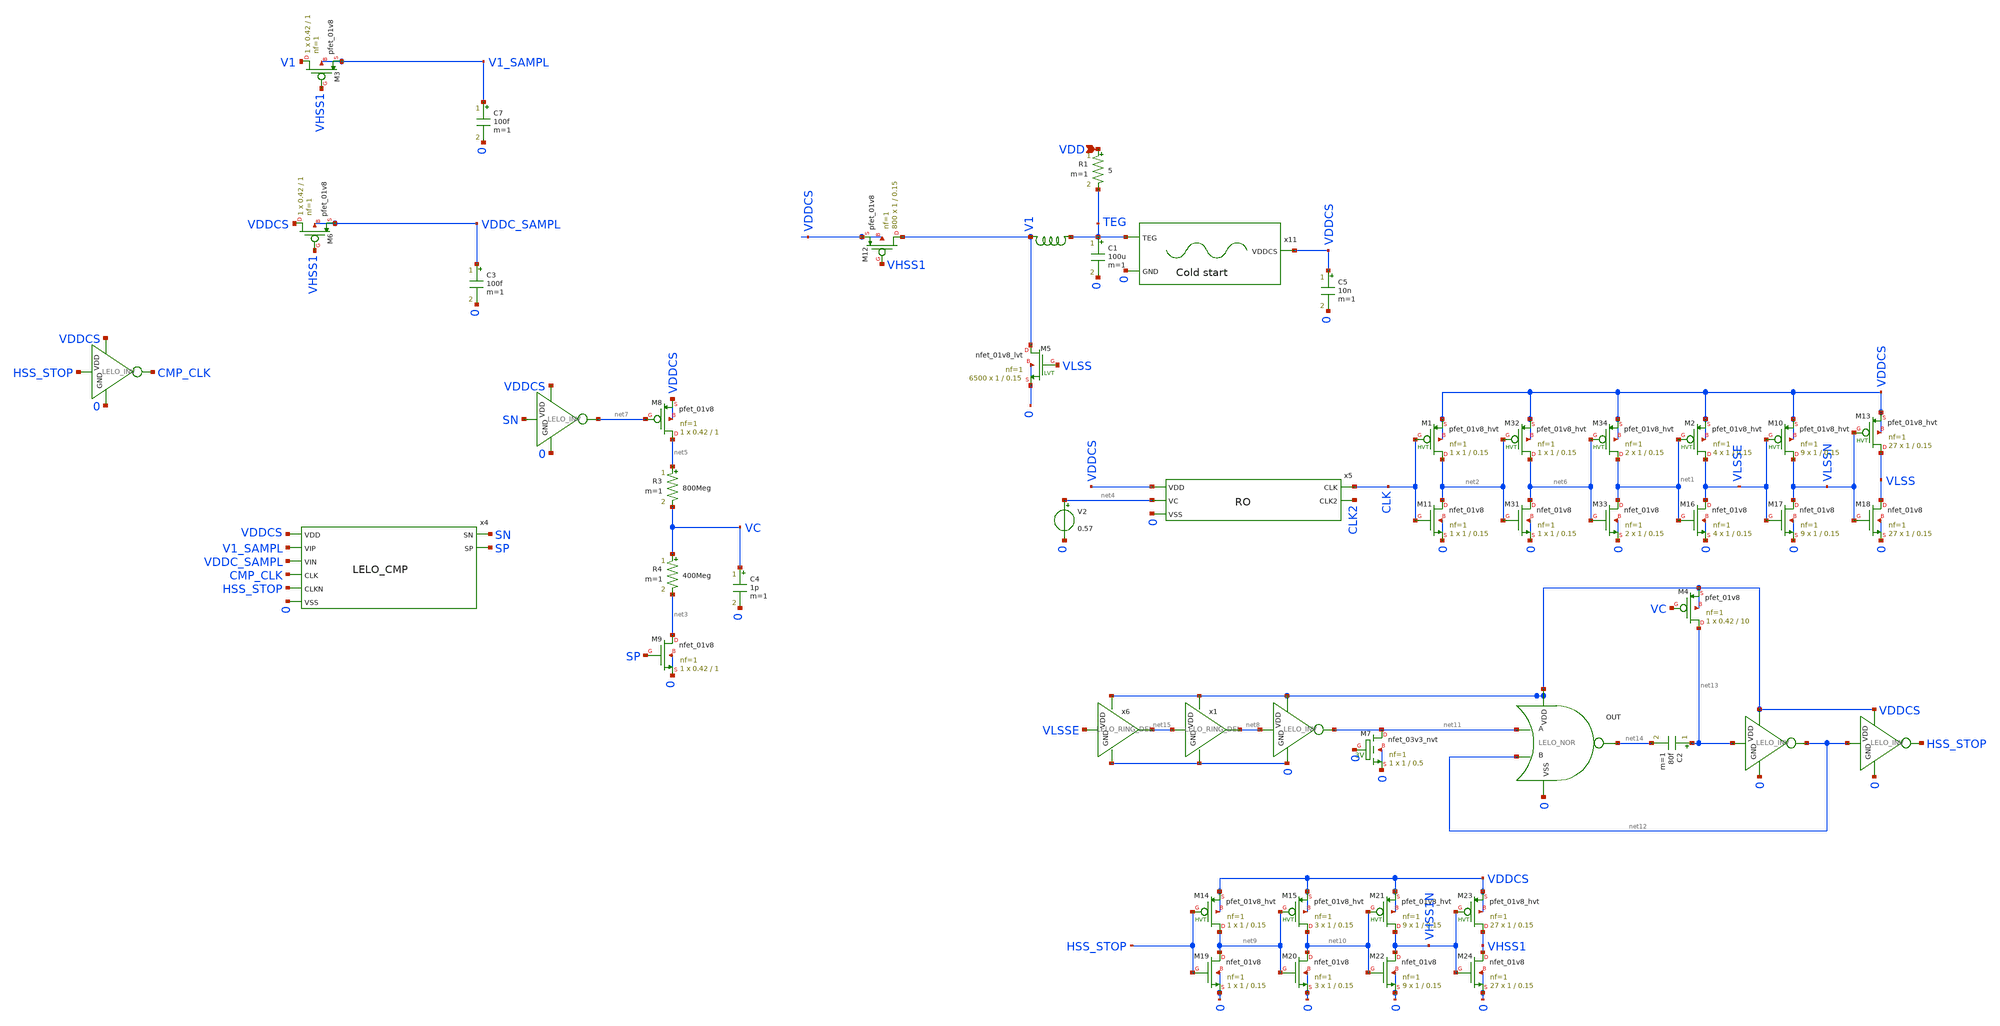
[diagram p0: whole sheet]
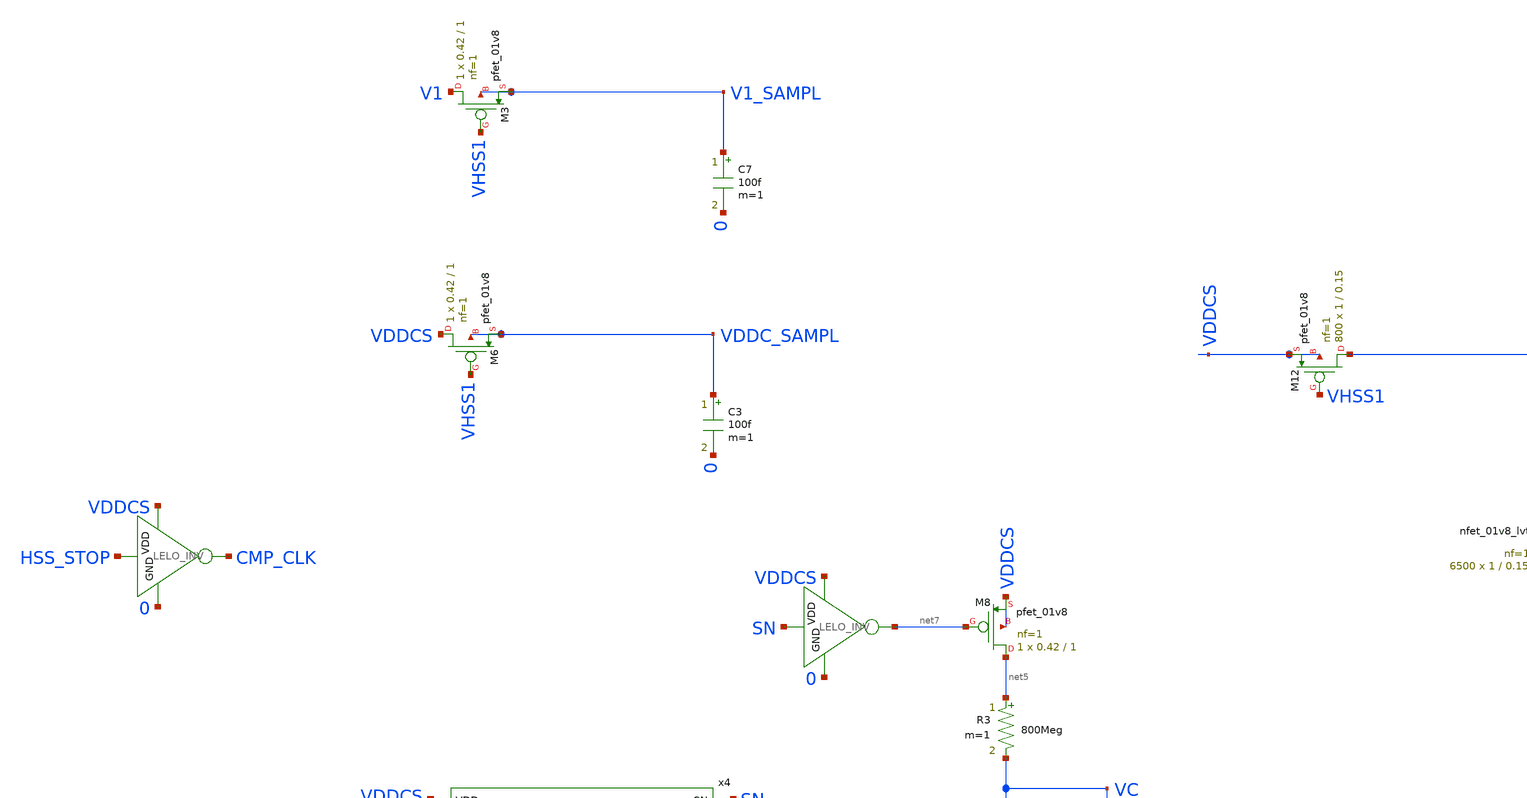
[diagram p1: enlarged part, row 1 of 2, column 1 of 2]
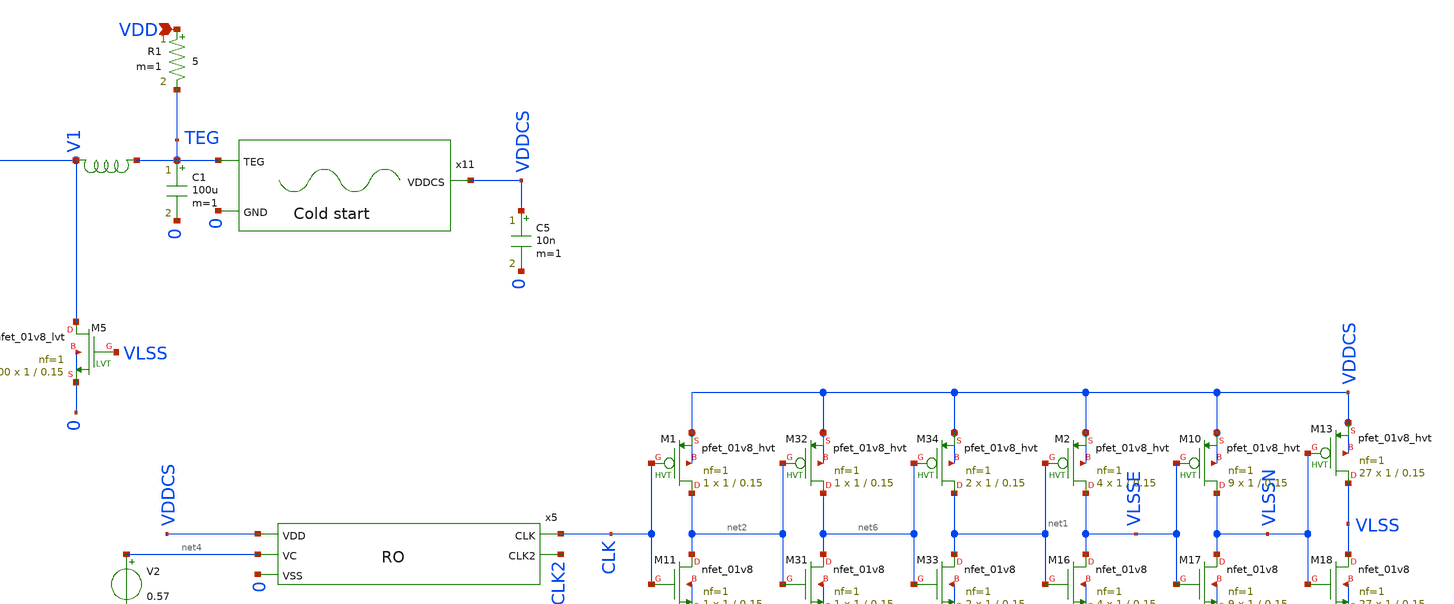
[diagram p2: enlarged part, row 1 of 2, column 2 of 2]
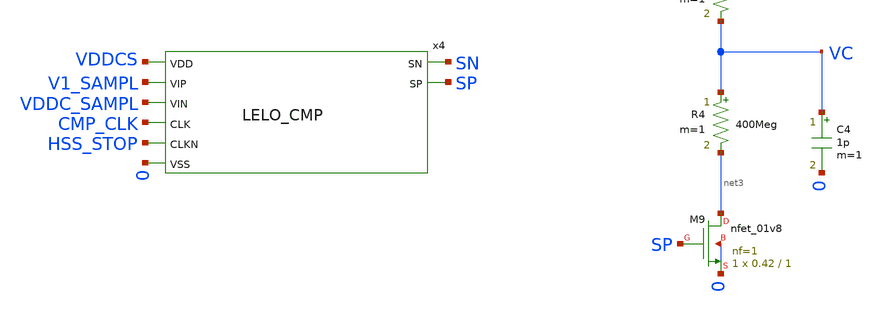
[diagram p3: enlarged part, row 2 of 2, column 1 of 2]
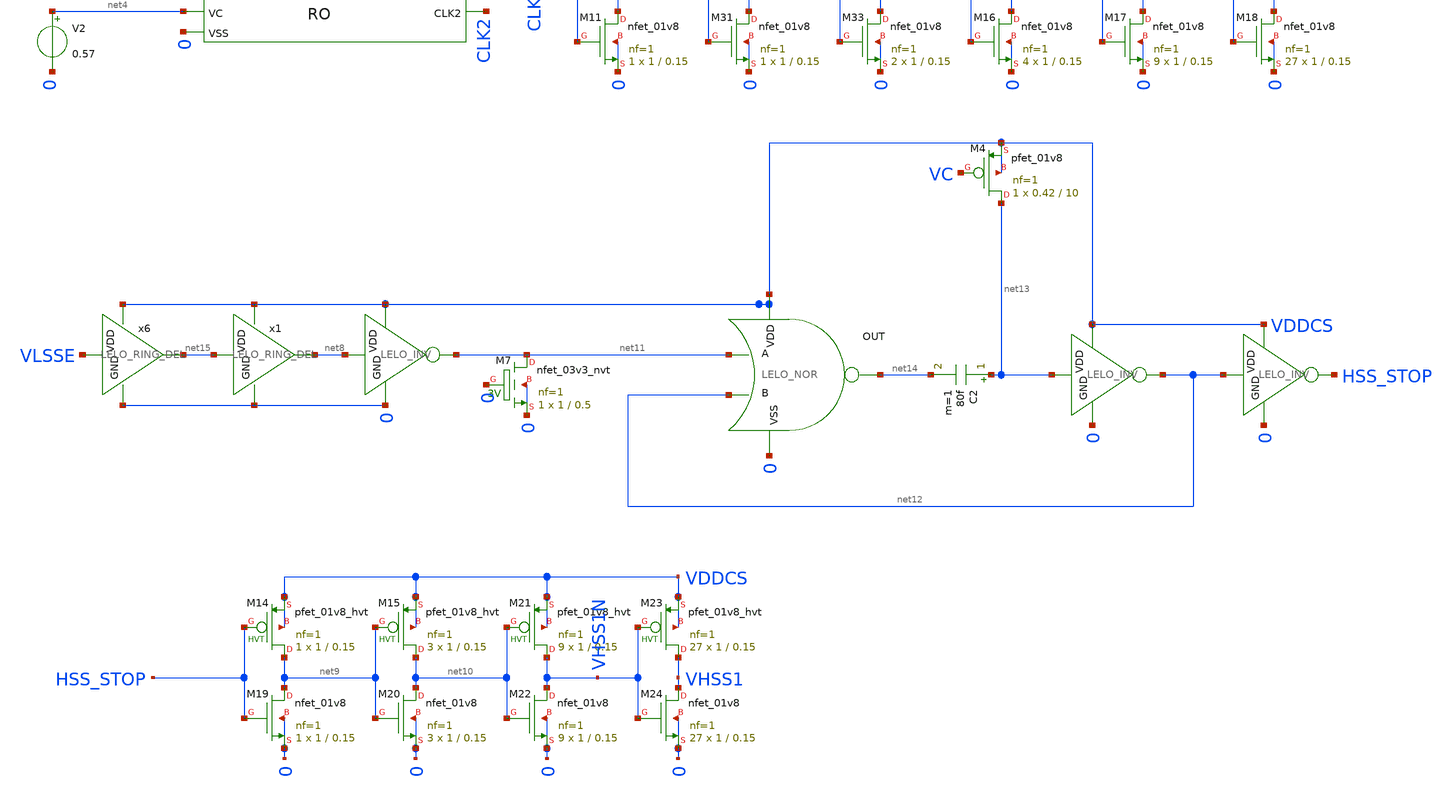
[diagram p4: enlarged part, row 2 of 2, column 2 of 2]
** sch_path: design/LELO_SVOD_SKY130A/LELO_EXSC.sch
**.subckt LELO_EXSC VDD
*.ipin VDD
R1 VDD TEG 5 m=1
C7 V1_SAMPL 0 100f m=1
x5 CLK CLK2 VDDCS net4 0 RO
XM12 V1 VHSS1 VDDCS VDDCS sky130_fd_pr__pfet_01v8 L=0.15 W=1 nf=1 ad='int((1 + 1)/2) * 1 / 1 * 0.29'
+ as='int((1 + 2)/2) * 1 / 1 * 0.29' pd='2*int((1 + 1)/2) * (1 / 1 + 0.29)' ps='2*int((1 + 2)/2) * (1 / 1 + 0.29)'
+ nrd='0.29 / 1 ' nrs='0.29 / 1 ' sa=0 sb=0 sd=0 mult=800 m=800
C1 TEG 0 100u m=1
XM5 V1 VLSS 0 0 sky130_fd_pr__nfet_01v8_lvt L=0.15 W=1 nf=1 ad='int((1 + 1)/2) * 1 / 1 * 0.29' as='int((1 + 2)/2) * 1 / 1 * 0.29'
+ pd='2*int((1 + 1)/2) * (1 / 1 + 0.29)' ps='2*int((1 + 2)/2) * (1 / 1 + 0.29)' nrd='0.29 / 1 ' nrs='0.29 / 1 '
+ sa=0 sb=0 sd=0 mult=6500 m=6500
x4 SN SP VDDCS V1_SAMPL VDDC_SAMPL CMP_CLK HSS_STOP 0 LELO_CMP
XM3 V1 VHSS1 V1_SAMPL V1_SAMPL sky130_fd_pr__pfet_01v8 L=1 W=0.42 nf=1 ad='int((1 + 1)/2) * 0.42 / 1 * 0.29'
+ as='int((1 + 2)/2) * 0.42 / 1 * 0.29' pd='2*int((1 + 1)/2) * (0.42 / 1 + 0.29)' ps='2*int((1 + 2)/2) * (0.42 / 1 + 0.29)'
+ nrd='0.29 / 0.42 ' nrs='0.29 / 0.42 ' sa=0 sb=0 sd=0 mult=1 m=1
C3 VDDC_SAMPL 0 100f m=1
XM6 VDDCS VHSS1 VDDC_SAMPL VDDC_SAMPL sky130_fd_pr__pfet_01v8 L=1 W=0.42 nf=1 ad='int((1 + 1)/2) * 0.42 / 1 * 0.29'
+ as='int((1 + 2)/2) * 0.42 / 1 * 0.29' pd='2*int((1 + 1)/2) * (0.42 / 1 + 0.29)' ps='2*int((1 + 2)/2) * (0.42 / 1 + 0.29)'
+ nrd='0.29 / 0.42 ' nrs='0.29 / 0.42 ' sa=0 sb=0 sd=0 mult=1 m=1
C4 VC 0 1p m=1
XM8 net5 net7 VDDCS VDDCS sky130_fd_pr__pfet_01v8 L=1 W=0.42 nf=1 ad='int((1 + 1)/2) * 0.42 / 1 * 0.29'
+ as='int((1 + 2)/2) * 0.42 / 1 * 0.29' pd='2*int((1 + 1)/2) * (0.42 / 1 + 0.29)' ps='2*int((1 + 2)/2) * (0.42 / 1 + 0.29)'
+ nrd='0.29 / 0.42 ' nrs='0.29 / 0.42 ' sa=0 sb=0 sd=0 mult=1 m=1
XM9 net3 SP 0 0 sky130_fd_pr__nfet_01v8 L=1 W=0.42 nf=1 ad='int((1 + 1)/2) * 0.42 / 1 * 0.29' as='int((1 + 2)/2) * 0.42 / 1 * 0.29'
+ pd='2*int((1 + 1)/2) * (0.42 / 1 + 0.29)' ps='2*int((1 + 2)/2) * (0.42 / 1 + 0.29)' nrd='0.29 / 0.42 '
+ nrs='0.29 / 0.42 ' sa=0 sb=0 sd=0 mult=1 m=1
V2 net4 0 0.57
x14 VDDCS HSS_STOP CMP_CLK 0 LELO_INV
R3 net5 VC 800Meg m=1
R4 VC net3 400Meg m=1
XM11 net2 CLK 0 0 sky130_fd_pr__nfet_01v8 L=0.15 W=1 nf=1 ad='int((1 + 1)/2) * 1 / 1 * 0.29' as='int((1 + 2)/2) * 1 / 1 * 0.29'
+ pd='2*int((1 + 1)/2) * (1 / 1 + 0.29)' ps='2*int((1 + 2)/2) * (1 / 1 + 0.29)' nrd='0.29 / 1 ' nrs='0.29 / 1 '
+ sa=0 sb=0 sd=0 mult=1 m=1
XM16 VLSSE net1 0 0 sky130_fd_pr__nfet_01v8 L=0.15 W=1 nf=1 ad='int((1 + 1)/2) * 1 / 1 * 0.29' as='int((1 + 2)/2) * 1 / 1 * 0.29'
+ pd='2*int((1 + 1)/2) * (1 / 1 + 0.29)' ps='2*int((1 + 2)/2) * (1 / 1 + 0.29)' nrd='0.29 / 1 ' nrs='0.29 / 1 '
+ sa=0 sb=0 sd=0 mult=4 m=4
XM17 VLSSN VLSSE 0 0 sky130_fd_pr__nfet_01v8 L=0.15 W=1 nf=1 ad='int((1 + 1)/2) * 1 / 1 * 0.29' as='int((1 + 2)/2) * 1 / 1 * 0.29'
+ pd='2*int((1 + 1)/2) * (1 / 1 + 0.29)' ps='2*int((1 + 2)/2) * (1 / 1 + 0.29)' nrd='0.29 / 1 ' nrs='0.29 / 1 '
+ sa=0 sb=0 sd=0 mult=9 m=9
XM18 VLSS VLSSN 0 0 sky130_fd_pr__nfet_01v8 L=0.15 W=1 nf=1 ad='int((1 + 1)/2) * 1 / 1 * 0.29' as='int((1 + 2)/2) * 1 / 1 * 0.29'
+ pd='2*int((1 + 1)/2) * (1 / 1 + 0.29)' ps='2*int((1 + 2)/2) * (1 / 1 + 0.29)' nrd='0.29 / 1 ' nrs='0.29 / 1 '
+ sa=0 sb=0 sd=0 mult=27 m=27
XM1 net2 CLK VDDCS VDDCS sky130_fd_pr__pfet_01v8_hvt L=0.15 W=1 nf=1 ad='int((1 + 1)/2) * 1 / 1 * 0.29'
+ as='int((1 + 2)/2) * 1 / 1 * 0.29' pd='2*int((1 + 1)/2) * (1 / 1 + 0.29)' ps='2*int((1 + 2)/2) * (1 / 1 + 0.29)'
+ nrd='0.29 / 1 ' nrs='0.29 / 1 ' sa=0 sb=0 sd=0 mult=1 m=1
XM2 VLSSE net1 VDDCS VDDCS sky130_fd_pr__pfet_01v8_hvt L=0.15 W=1 nf=1 ad='int((1 + 1)/2) * 1 / 1 * 0.29'
+ as='int((1 + 2)/2) * 1 / 1 * 0.29' pd='2*int((1 + 1)/2) * (1 / 1 + 0.29)' ps='2*int((1 + 2)/2) * (1 / 1 + 0.29)'
+ nrd='0.29 / 1 ' nrs='0.29 / 1 ' sa=0 sb=0 sd=0 mult=4 m=4
XM10 VLSSN VLSSE VDDCS VDDCS sky130_fd_pr__pfet_01v8_hvt L=0.15 W=1 nf=1 ad='int((1 + 1)/2) * 1 / 1 * 0.29'
+ as='int((1 + 2)/2) * 1 / 1 * 0.29' pd='2*int((1 + 1)/2) * (1 / 1 + 0.29)' ps='2*int((1 + 2)/2) * (1 / 1 + 0.29)'
+ nrd='0.29 / 1 ' nrs='0.29 / 1 ' sa=0 sb=0 sd=0 mult=9 m=9
XM13 VLSS VLSSN VDDCS VDDCS sky130_fd_pr__pfet_01v8_hvt L=0.15 W=1 nf=1 ad='int((1 + 1)/2) * 1 / 1 * 0.29'
+ as='int((1 + 2)/2) * 1 / 1 * 0.29' pd='2*int((1 + 1)/2) * (1 / 1 + 0.29)' ps='2*int((1 + 2)/2) * (1 / 1 + 0.29)'
+ nrd='0.29 / 1 ' nrs='0.29 / 1 ' sa=0 sb=0 sd=0 mult=27 m=27
XM31 net6 net2 0 0 sky130_fd_pr__nfet_01v8 L=0.15 W=1 nf=1 ad='int((1 + 1)/2) * 1 / 1 * 0.29' as='int((1 + 2)/2) * 1 / 1 * 0.29'
+ pd='2*int((1 + 1)/2) * (1 / 1 + 0.29)' ps='2*int((1 + 2)/2) * (1 / 1 + 0.29)' nrd='0.29 / 1 ' nrs='0.29 / 1 '
+ sa=0 sb=0 sd=0 mult=1 m=1
XM32 net6 net2 VDDCS VDDCS sky130_fd_pr__pfet_01v8_hvt L=0.15 W=1 nf=1 ad='int((1 + 1)/2) * 1 / 1 * 0.29'
+ as='int((1 + 2)/2) * 1 / 1 * 0.29' pd='2*int((1 + 1)/2) * (1 / 1 + 0.29)' ps='2*int((1 + 2)/2) * (1 / 1 + 0.29)'
+ nrd='0.29 / 1 ' nrs='0.29 / 1 ' sa=0 sb=0 sd=0 mult=1 m=1
XM33 net1 net6 0 0 sky130_fd_pr__nfet_01v8 L=0.15 W=1 nf=1 ad='int((1 + 1)/2) * 1 / 1 * 0.29' as='int((1 + 2)/2) * 1 / 1 * 0.29'
+ pd='2*int((1 + 1)/2) * (1 / 1 + 0.29)' ps='2*int((1 + 2)/2) * (1 / 1 + 0.29)' nrd='0.29 / 1 ' nrs='0.29 / 1 '
+ sa=0 sb=0 sd=0 mult=2 m=2
XM34 net1 net6 VDDCS VDDCS sky130_fd_pr__pfet_01v8_hvt L=0.15 W=1 nf=1 ad='int((1 + 1)/2) * 1 / 1 * 0.29'
+ as='int((1 + 2)/2) * 1 / 1 * 0.29' pd='2*int((1 + 1)/2) * (1 / 1 + 0.29)' ps='2*int((1 + 2)/2) * (1 / 1 + 0.29)'
+ nrd='0.29 / 1 ' nrs='0.29 / 1 ' sa=0 sb=0 sd=0 mult=2 m=2
x7 TEG V1 XGL6030-822_sat
x10 VDDCS SN net7 0 LELO_INV
C5 VDDCS 0 10n m=1
x11 TEG VDDCS 0 LELO_COLD_START
x16 VDDCS net12 HSS_STOP 0 LELO_INV
x9 VDDCS net8 net11 0 LELO_INV
XM19 net9 HSS_STOP 0 0 sky130_fd_pr__nfet_01v8 L=0.15 W=1 nf=1 ad='int((1 + 1)/2) * 1 / 1 * 0.29' as='int((1 + 2)/2) * 1 / 1 * 0.29'
+ pd='2*int((1 + 1)/2) * (1 / 1 + 0.29)' ps='2*int((1 + 2)/2) * (1 / 1 + 0.29)' nrd='0.29 / 1 ' nrs='0.29 / 1 '
+ sa=0 sb=0 sd=0 mult=1 m=1
XM20 net10 net9 0 0 sky130_fd_pr__nfet_01v8 L=0.15 W=1 nf=1 ad='int((1 + 1)/2) * 1 / 1 * 0.29' as='int((1 + 2)/2) * 1 / 1 * 0.29'
+ pd='2*int((1 + 1)/2) * (1 / 1 + 0.29)' ps='2*int((1 + 2)/2) * (1 / 1 + 0.29)' nrd='0.29 / 1 ' nrs='0.29 / 1 '
+ sa=0 sb=0 sd=0 mult=3 m=3
XM22 VHSS1N net10 0 0 sky130_fd_pr__nfet_01v8 L=0.15 W=1 nf=1 ad='int((1 + 1)/2) * 1 / 1 * 0.29' as='int((1 + 2)/2) * 1 / 1 * 0.29'
+ pd='2*int((1 + 1)/2) * (1 / 1 + 0.29)' ps='2*int((1 + 2)/2) * (1 / 1 + 0.29)' nrd='0.29 / 1 ' nrs='0.29 / 1 '
+ sa=0 sb=0 sd=0 mult=9 m=9
XM24 VHSS1 VHSS1N 0 0 sky130_fd_pr__nfet_01v8 L=0.15 W=1 nf=1 ad='int((1 + 1)/2) * 1 / 1 * 0.29' as='int((1 + 2)/2) * 1 / 1 * 0.29'
+ pd='2*int((1 + 1)/2) * (1 / 1 + 0.29)' ps='2*int((1 + 2)/2) * (1 / 1 + 0.29)' nrd='0.29 / 1 ' nrs='0.29 / 1 '
+ sa=0 sb=0 sd=0 mult=27 m=27
XM14 net9 HSS_STOP VDDCS VDDCS sky130_fd_pr__pfet_01v8_hvt L=0.15 W=1 nf=1 ad='int((1 + 1)/2) * 1 / 1 * 0.29'
+ as='int((1 + 2)/2) * 1 / 1 * 0.29' pd='2*int((1 + 1)/2) * (1 / 1 + 0.29)' ps='2*int((1 + 2)/2) * (1 / 1 + 0.29)'
+ nrd='0.29 / 1 ' nrs='0.29 / 1 ' sa=0 sb=0 sd=0 mult=1 m=1
XM15 net10 net9 VDDCS VDDCS sky130_fd_pr__pfet_01v8_hvt L=0.15 W=1 nf=1 ad='int((1 + 1)/2) * 1 / 1 * 0.29'
+ as='int((1 + 2)/2) * 1 / 1 * 0.29' pd='2*int((1 + 1)/2) * (1 / 1 + 0.29)' ps='2*int((1 + 2)/2) * (1 / 1 + 0.29)'
+ nrd='0.29 / 1 ' nrs='0.29 / 1 ' sa=0 sb=0 sd=0 mult=3 m=3
XM21 VHSS1N net10 VDDCS VDDCS sky130_fd_pr__pfet_01v8_hvt L=0.15 W=1 nf=1 ad='int((1 + 1)/2) * 1 / 1 * 0.29'
+ as='int((1 + 2)/2) * 1 / 1 * 0.29' pd='2*int((1 + 1)/2) * (1 / 1 + 0.29)' ps='2*int((1 + 2)/2) * (1 / 1 + 0.29)'
+ nrd='0.29 / 1 ' nrs='0.29 / 1 ' sa=0 sb=0 sd=0 mult=9 m=9
XM23 VHSS1 VHSS1N VDDCS VDDCS sky130_fd_pr__pfet_01v8_hvt L=0.15 W=1 nf=1 ad='int((1 + 1)/2) * 1 / 1 * 0.29'
+ as='int((1 + 2)/2) * 1 / 1 * 0.29' pd='2*int((1 + 1)/2) * (1 / 1 + 0.29)' ps='2*int((1 + 2)/2) * (1 / 1 + 0.29)'
+ nrd='0.29 / 1 ' nrs='0.29 / 1 ' sa=0 sb=0 sd=0 mult=27 m=27
x2 VDDCS net14 net11 net12 0 LELO_NOR
C2 net13 net14 80f m=1
x3 VDDCS net13 net12 0 LELO_INV
XM4 net13 VC VDDCS VDDCS sky130_fd_pr__pfet_01v8 L=10 W=0.42 nf=1 ad='int((1 + 1)/2) * 0.42 / 1 * 0.29'
+ as='int((1 + 2)/2) * 0.42 / 1 * 0.29' pd='2*int((1 + 1)/2) * (0.42 / 1 + 0.29)' ps='2*int((1 + 2)/2) * (0.42 / 1 + 0.29)'
+ nrd='0.29 / 0.42 ' nrs='0.29 / 0.42 ' sa=0 sb=0 sd=0 mult=1 m=1
x1 VDDCS net15 net8 0 LELO_RING_DEL
x6 VDDCS VLSSE net15 0 LELO_RING_DEL
XM7 net11 0 0 0 sky130_fd_pr__nfet_03v3_nvt L=0.5 W=1 nf=1 ad='int((1 + 1)/2) * 1 / 1 * 0.29' as='int((1 + 2)/2) * 1 / 1 * 0.29'
+ pd='2*int((1 + 1)/2) * (1 / 1 + 0.29)' ps='2*int((1 + 2)/2) * (1 / 1 + 0.29)' nrd='0.29 / 1 ' nrs='0.29 / 1 '
+ sa=0 sb=0 sd=0 mult=1 m=1
**.ends

* expanding   symbol:  LELO_SVOD_SKY130A/RO.sym # of pins=5
** sym_path: design/LELO_SVOD_SKY130A/RO.sym
** sch_path: design/LELO_SVOD_SKY130A/RO.sch
.subckt RO CLK CLK2 VDD VC VSS
*.opin CLK
*.ipin VSS
*.opin CLK2
*.ipin VDD
*.ipin VC
x1 VDD VC2 CLK net1 VC VSS LELO_RING_DEL_VC
x2 VDD VC2 net1 net2 VC VSS LELO_RING_DEL_VC
x3 VDD VC2 net2 net3 VC VSS LELO_RING_DEL_VC
x4 VDD VC2 net3 CLK2 VC VSS LELO_RING_DEL_VC
x5 VDD VC2 CLK2 net4 VC VSS LELO_RING_DEL_VC
x6 VDD VC2 net4 net5 VC VSS LELO_RING_DEL_VC
x7 VDD VC2 net5 CLK VC VSS LELO_RING_DEL_VC
XM1 VC2 VC VSS VSS sky130_fd_pr__nfet_01v8 L=5 W=0.42 nf=1 ad='int((1 + 1)/2) * 0.42 / 1 * 0.29' as='int((1 + 2)/2) * 0.42 / 1 * 0.29'
+ pd='2*int((1 + 1)/2) * (0.42 / 1 + 0.29)' ps='2*int((1 + 2)/2) * (0.42 / 1 + 0.29)' nrd='0.29 / 0.42 '
+ nrs='0.29 / 0.42 ' sa=0 sb=0 sd=0 mult=1 m=1
XM2 VC2 VC2 VDD VDD sky130_fd_pr__pfet_01v8 L=5 W=0.42 nf=1 ad='int((1 + 1)/2) * 0.42 / 1 * 0.29' as='int((1 + 2)/2) * 0.42 / 1 * 0.29'
+ pd='2*int((1 + 1)/2) * (0.42 / 1 + 0.29)' ps='2*int((1 + 2)/2) * (0.42 / 1 + 0.29)' nrd='0.29 / 0.42 '
+ nrs='0.29 / 0.42 ' sa=0 sb=0 sd=0 mult=1 m=1
.ends


* expanding   symbol:  LELO_SVOD_SKY130A/LELO_CMP.sym # of pins=8
** sym_path: design/LELO_SVOD_SKY130A/LELO_CMP.sym
** sch_path: design/LELO_SVOD_SKY130A/LELO_CMP.sch
.subckt LELO_CMP SN SP VDD VIP VIN CLK CLKN VSS
*.ipin VIP
*.ipin VIN
*.ipin CLK
*.ipin CLKN
*.ipin VDD
*.ipin VSS
*.opin SN
*.opin SP
XM2 SN net3 net5 VDD sky130_fd_pr__pfet_01v8_lvt L=0.44 W=1.92 nf=2 ad='int((2 + 1)/2) * 1.92 / 2 * 0.29'
+ as='int((2 + 2)/2) * 1.92 / 2 * 0.29' pd='2*int((2 + 1)/2) * (1.92 / 2 + 0.29)' ps='2*int((2 + 2)/2) * (1.92 / 2 + 0.29)'
+ nrd='0.29 / 1.92 ' nrs='0.29 / 1.92 ' sa=0 sb=0 sd=0 mult=3 m=3
XM1 SP net2 net6 VDD sky130_fd_pr__pfet_01v8_lvt L=0.44 W=1.92 nf=2 ad='int((2 + 1)/2) * 1.92 / 2 * 0.29'
+ as='int((2 + 2)/2) * 1.92 / 2 * 0.29' pd='2*int((2 + 1)/2) * (1.92 / 2 + 0.29)' ps='2*int((2 + 2)/2) * (1.92 / 2 + 0.29)'
+ nrd='0.29 / 1.92 ' nrs='0.29 / 1.92 ' sa=0 sb=0 sd=0 mult=3 m=3
XM3 net2 VIP net1 VSS sky130_fd_pr__nfet_01v8_lvt L=0.44 W=6.4 nf=1 ad='int((1 + 1)/2) * 6.4 / 1 * 0.29'
+ as='int((1 + 2)/2) * 6.4 / 1 * 0.29' pd='2*int((1 + 1)/2) * (6.4 / 1 + 0.29)' ps='2*int((1 + 2)/2) * (6.4 / 1 + 0.29)'
+ nrd='0.29 / 6.4 ' nrs='0.29 / 6.4 ' sa=0 sb=0 sd=0 mult=1 m=1
XM4 net3 VIN net1 VSS sky130_fd_pr__nfet_01v8_lvt L=0.44 W=6.4 nf=1 ad='int((1 + 1)/2) * 6.4 / 1 * 0.29'
+ as='int((1 + 2)/2) * 6.4 / 1 * 0.29' pd='2*int((1 + 1)/2) * (6.4 / 1 + 0.29)' ps='2*int((1 + 2)/2) * (6.4 / 1 + 0.29)'
+ nrd='0.29 / 6.4 ' nrs='0.29 / 6.4 ' sa=0 sb=0 sd=0 mult=1 m=1
XM5 net3 CLK VDD VDD sky130_fd_pr__pfet_01v8_lvt L=0.94 W=1.92 nf=2 ad='int((2 + 1)/2) * 1.92 / 2 * 0.29'
+ as='int((2 + 2)/2) * 1.92 / 2 * 0.29' pd='2*int((2 + 1)/2) * (1.92 / 2 + 0.29)' ps='2*int((2 + 2)/2) * (1.92 / 2 + 0.29)'
+ nrd='0.29 / 1.92 ' nrs='0.29 / 1.92 ' sa=0 sb=0 sd=0 mult=1 m=1
XM6 net6 SN VDD VDD sky130_fd_pr__pfet_01v8_lvt L=0.94 W=1.92 nf=2 ad='int((2 + 1)/2) * 1.92 / 2 * 0.29'
+ as='int((2 + 2)/2) * 1.92 / 2 * 0.29' pd='2*int((2 + 1)/2) * (1.92 / 2 + 0.29)' ps='2*int((2 + 2)/2) * (1.92 / 2 + 0.29)'
+ nrd='0.29 / 1.92 ' nrs='0.29 / 1.92 ' sa=0 sb=0 sd=0 mult=1 m=1
XM7 net5 SP VDD VDD sky130_fd_pr__pfet_01v8_lvt L=0.94 W=1.92 nf=2 ad='int((2 + 1)/2) * 1.92 / 2 * 0.29'
+ as='int((2 + 2)/2) * 1.92 / 2 * 0.29' pd='2*int((2 + 1)/2) * (1.92 / 2 + 0.29)' ps='2*int((2 + 2)/2) * (1.92 / 2 + 0.29)'
+ nrd='0.29 / 1.92 ' nrs='0.29 / 1.92 ' sa=0 sb=0 sd=0 mult=1 m=1
XM8 net2 CLK VDD VDD sky130_fd_pr__pfet_01v8_lvt L=0.94 W=1.92 nf=2 ad='int((2 + 1)/2) * 1.92 / 2 * 0.29'
+ as='int((2 + 2)/2) * 1.92 / 2 * 0.29' pd='2*int((2 + 1)/2) * (1.92 / 2 + 0.29)' ps='2*int((2 + 2)/2) * (1.92 / 2 + 0.29)'
+ nrd='0.29 / 1.92 ' nrs='0.29 / 1.92 ' sa=0 sb=0 sd=0 mult=1 m=1
XM9 net1 CLK net4 VSS sky130_fd_pr__nfet_01v8 L=0.94 W=1.92 nf=2 ad='int((2 + 1)/2) * 1.92 / 2 * 0.29'
+ as='int((2 + 2)/2) * 1.92 / 2 * 0.29' pd='2*int((2 + 1)/2) * (1.92 / 2 + 0.29)' ps='2*int((2 + 2)/2) * (1.92 / 2 + 0.29)'
+ nrd='0.29 / 1.92 ' nrs='0.29 / 1.92 ' sa=0 sb=0 sd=0 mult=1 m=1
XM10 net4 CLK VSS VSS sky130_fd_pr__nfet_01v8 L=0.94 W=1.92 nf=2 ad='int((2 + 1)/2) * 1.92 / 2 * 0.29'
+ as='int((2 + 2)/2) * 1.92 / 2 * 0.29' pd='2*int((2 + 1)/2) * (1.92 / 2 + 0.29)' ps='2*int((2 + 2)/2) * (1.92 / 2 + 0.29)'
+ nrd='0.29 / 1.92 ' nrs='0.29 / 1.92 ' sa=0 sb=0 sd=0 mult=1 m=1
XM11 SN CLKN VSS VSS sky130_fd_pr__nfet_01v8 L=0.94 W=1.92 nf=2 ad='int((2 + 1)/2) * 1.92 / 2 * 0.29'
+ as='int((2 + 2)/2) * 1.92 / 2 * 0.29' pd='2*int((2 + 1)/2) * (1.92 / 2 + 0.29)' ps='2*int((2 + 2)/2) * (1.92 / 2 + 0.29)'
+ nrd='0.29 / 1.92 ' nrs='0.29 / 1.92 ' sa=0 sb=0 sd=0 mult=1 m=1
XM12 SP SN VSS VSS sky130_fd_pr__nfet_01v8 L=0.94 W=1.92 nf=2 ad='int((2 + 1)/2) * 1.92 / 2 * 0.29' as='int((2 + 2)/2) * 1.92 / 2 * 0.29'
+ pd='2*int((2 + 1)/2) * (1.92 / 2 + 0.29)' ps='2*int((2 + 2)/2) * (1.92 / 2 + 0.29)' nrd='0.29 / 1.92 '
+ nrs='0.29 / 1.92 ' sa=0 sb=0 sd=0 mult=1 m=1
XM13 SN SP VSS VSS sky130_fd_pr__nfet_01v8 L=0.94 W=1.92 nf=2 ad='int((2 + 1)/2) * 1.92 / 2 * 0.29' as='int((2 + 2)/2) * 1.92 / 2 * 0.29'
+ pd='2*int((2 + 1)/2) * (1.92 / 2 + 0.29)' ps='2*int((2 + 2)/2) * (1.92 / 2 + 0.29)' nrd='0.29 / 1.92 '
+ nrs='0.29 / 1.92 ' sa=0 sb=0 sd=0 mult=1 m=1
XM14 SP CLKN VSS VSS sky130_fd_pr__nfet_01v8 L=0.94 W=1.92 nf=2 ad='int((2 + 1)/2) * 1.92 / 2 * 0.29'
+ as='int((2 + 2)/2) * 1.92 / 2 * 0.29' pd='2*int((2 + 1)/2) * (1.92 / 2 + 0.29)' ps='2*int((2 + 2)/2) * (1.92 / 2 + 0.29)'
+ nrd='0.29 / 1.92 ' nrs='0.29 / 1.92 ' sa=0 sb=0 sd=0 mult=1 m=1
.ends


* expanding   symbol:  LELO_SVOD_SKY130A/LELO_INV.sym # of pins=4
** sym_path: design/LELO_SVOD_SKY130A/LELO_INV.sym
** sch_path: design/LELO_SVOD_SKY130A/LELO_INV.sch
.subckt LELO_INV VDD VIN VOUT GND
*.ipin VIN
*.ipin VDD
*.ipin GND
*.opin VOUT
XM1 VOUT VIN GND GND sky130_fd_pr__nfet_01v8_lvt L=0.15 W=1 nf=1 ad='int((1 + 1)/2) * 1 / 1 * 0.29' as='int((1 + 2)/2) * 1 / 1 * 0.29'
+ pd='2*int((1 + 1)/2) * (1 / 1 + 0.29)' ps='2*int((1 + 2)/2) * (1 / 1 + 0.29)' nrd='0.29 / 1 ' nrs='0.29 / 1 '
+ sa=0 sb=0 sd=0 mult=1 m=1
XM2 VOUT VIN VDD VDD sky130_fd_pr__pfet_01v8_lvt L=0.35 W=1 nf=1 ad='int((1 + 1)/2) * 1 / 1 * 0.29' as='int((1 + 2)/2) * 1 / 1 * 0.29'
+ pd='2*int((1 + 1)/2) * (1 / 1 + 0.29)' ps='2*int((1 + 2)/2) * (1 / 1 + 0.29)' nrd='0.29 / 1 ' nrs='0.29 / 1 '
+ sa=0 sb=0 sd=0 mult=2 m=2
.ends


* expanding   symbol:  LELO_SVOD_SKY130A/XGL6030-822_sat.sym # of pins=2
** sym_path: design/LELO_SVOD_SKY130A/XGL6030-822_sat.sym

.subckt XGL6030-822_sat port1 port2
X1 port1 port2 Model1C R1=5 R2=0.04 C= 15.2p K1=0.000001 K2=2 K3= 8.2u K4=0.000001 K5=0.000001
+ L=8.1093E-06 Is=13.9236 a=0.7109 L_Z0=0 L_EL=0 L_F0=0E6 PkZ=7057.14402
.ends XGL6030-822_sat


* expanding   symbol:  LELO_SVOD_SKY130A/LELO_COLD_START.sym # of pins=3
** sym_path: design/LELO_SVOD_SKY130A/LELO_COLD_START.sym
** sch_path: design/LELO_SVOD_SKY130A/LELO_COLD_START.sch
.subckt LELO_COLD_START TEG VDDCS GND
*.ipin GND
*.ipin TEG
*.opin VDDCS
C2 net4 VG1 110p m=1
x1 VG2 net2 1812PS-564_imp
x2 net1 VG1 1812PS-564_imp
C4 net3 VG2 110p m=1
XM1 net1 VG2 GND GND sky130_fd_pr__nfet_20v0_zvt W=60 L=0.5 m=100
XM2 net2 VG1 GND GND sky130_fd_pr__nfet_20v0_zvt W=60 L=0.5 m=100
XM3 TEG TEG net4 TEG sky130_fd_pr__nfet_01v8_lvt L=0.15 W=10 nf=1 ad='int((1 + 1)/2) * 10 / 1 * 0.29'
+ as='int((1 + 2)/2) * 10 / 1 * 0.29' pd='2*int((1 + 1)/2) * (10 / 1 + 0.29)' ps='2*int((1 + 2)/2) * (10 / 1 + 0.29)'
+ nrd='0.29 / 10 ' nrs='0.29 / 10 ' sa=0 sb=0 sd=0 mult=1 m=1
XM7 net4 net4 net3 net4 sky130_fd_pr__nfet_01v8_lvt L=0.15 W=10 nf=1 ad='int((1 + 1)/2) * 10 / 1 * 0.29'
+ as='int((1 + 2)/2) * 10 / 1 * 0.29' pd='2*int((1 + 1)/2) * (10 / 1 + 0.29)' ps='2*int((1 + 2)/2) * (10 / 1 + 0.29)'
+ nrd='0.29 / 10 ' nrs='0.29 / 10 ' sa=0 sb=0 sd=0 mult=1 m=1
XM8 net3 net3 VDDCS net3 sky130_fd_pr__nfet_01v8_lvt L=0.15 W=10 nf=1 ad='int((1 + 1)/2) * 10 / 1 * 0.29'
+ as='int((1 + 2)/2) * 10 / 1 * 0.29' pd='2*int((1 + 1)/2) * (10 / 1 + 0.29)' ps='2*int((1 + 2)/2) * (10 / 1 + 0.29)'
+ nrd='0.29 / 10 ' nrs='0.29 / 10 ' sa=0 sb=0 sd=0 mult=1 m=1
x3 TEG net2 XGL6030-472_sat
x4 TEG net1 XGL6030-472_sat
.ends


* expanding   symbol:  LELO_SVOD_SKY130A/LELO_NOR.sym # of pins=5
** sym_path: design/LELO_SVOD_SKY130A/LELO_NOR.sym
** sch_path: design/LELO_SVOD_SKY130A/LELO_NOR.sch
.subckt LELO_NOR VDD OUT A B VSS
*.ipin VDD
*.ipin VSS
*.opin OUT
*.ipin A
*.ipin B
XM2 OUT B VSS VSS sky130_fd_pr__nfet_01v8 L=0.15 W=2 nf=1 ad='int((1 + 1)/2) * 2 / 1 * 0.29' as='int((1 + 2)/2) * 2 / 1 * 0.29'
+ pd='2*int((1 + 1)/2) * (2 / 1 + 0.29)' ps='2*int((1 + 2)/2) * (2 / 1 + 0.29)' nrd='0.29 / 2 ' nrs='0.29 / 2 '
+ sa=0 sb=0 sd=0 mult=1 m=1
XM1 OUT A VSS VSS sky130_fd_pr__nfet_01v8 L=0.15 W=2 nf=1 ad='int((1 + 1)/2) * 2 / 1 * 0.29' as='int((1 + 2)/2) * 2 / 1 * 0.29'
+ pd='2*int((1 + 1)/2) * (2 / 1 + 0.29)' ps='2*int((1 + 2)/2) * (2 / 1 + 0.29)' nrd='0.29 / 2 ' nrs='0.29 / 2 '
+ sa=0 sb=0 sd=0 mult=1 m=1
XM3 OUT B net1 VDD sky130_fd_pr__pfet_01v8 L=0.15 W=4 nf=1 ad='int((1 + 1)/2) * 4 / 1 * 0.29' as='int((1 + 2)/2) * 4 / 1 * 0.29'
+ pd='2*int((1 + 1)/2) * (4 / 1 + 0.29)' ps='2*int((1 + 2)/2) * (4 / 1 + 0.29)' nrd='0.29 / 4 ' nrs='0.29 / 4 '
+ sa=0 sb=0 sd=0 mult=1 m=1
XM4 net1 A VDD VDD sky130_fd_pr__pfet_01v8 L=0.15 W=4 nf=1 ad='int((1 + 1)/2) * 4 / 1 * 0.29' as='int((1 + 2)/2) * 4 / 1 * 0.29'
+ pd='2*int((1 + 1)/2) * (4 / 1 + 0.29)' ps='2*int((1 + 2)/2) * (4 / 1 + 0.29)' nrd='0.29 / 4 ' nrs='0.29 / 4 '
+ sa=0 sb=0 sd=0 mult=1 m=1
.ends


* expanding   symbol:  LELO_SVOD_SKY130A/LELO_RING_DEL.sym # of pins=4
** sym_path: design/LELO_SVOD_SKY130A/LELO_RING_DEL.sym
** sch_path: design/LELO_SVOD_SKY130A/LELO_RING_DEL.sch
.subckt LELO_RING_DEL VDD VIN VOUT GND
*.ipin VIN
*.ipin VDD
*.ipin GND
*.opin VOUT
XM1 VOUT VIN VDD VDD sky130_fd_pr__pfet_01v8_hvt L=1.7 W=0.42 nf=1 ad='int((1 + 1)/2) * 0.42 / 1 * 0.29'
+ as='int((1 + 2)/2) * 0.42 / 1 * 0.29' pd='2*int((1 + 1)/2) * (0.42 / 1 + 0.29)' ps='2*int((1 + 2)/2) * (0.42 / 1 + 0.29)'
+ nrd='0.29 / 0.42 ' nrs='0.29 / 0.42 ' sa=0 sb=0 sd=0 mult=1 m=1
XM2 VOUT VIN GND GND sky130_fd_pr__nfet_01v8 L=1.7 W=0.42 nf=1 ad='int((1 + 1)/2) * 0.42 / 1 * 0.29'
+ as='int((1 + 2)/2) * 0.42 / 1 * 0.29' pd='2*int((1 + 1)/2) * (0.42 / 1 + 0.29)' ps='2*int((1 + 2)/2) * (0.42 / 1 + 0.29)'
+ nrd='0.29 / 0.42 ' nrs='0.29 / 0.42 ' sa=0 sb=0 sd=0 mult=1 m=1
.ends


* expanding   symbol:  LELO_SVOD_SKY130A/LELO_RING_DEL_VC.sym # of pins=6
** sym_path: design/LELO_SVOD_SKY130A/LELO_RING_DEL_VC.sym
** sch_path: design/LELO_SVOD_SKY130A/LELO_RING_DEL_VC.sch
.subckt LELO_RING_DEL_VC VDD VC2 VIN VOUT VC GND
*.ipin VIN
*.ipin VDD
*.ipin GND
*.opin VOUT
*.ipin VC
*.ipin VC2
XM3 VOUT VIN net1 GND sky130_fd_pr__nfet_01v8 L=1 W=0.42 nf=1 ad='int((1 + 1)/2) * 0.42 / 1 * 0.29' as='int((1 + 2)/2) * 0.42 / 1 * 0.29'
+ pd='2*int((1 + 1)/2) * (0.42 / 1 + 0.29)' ps='2*int((1 + 2)/2) * (0.42 / 1 + 0.29)' nrd='0.29 / 0.42 '
+ nrs='0.29 / 0.42 ' sa=0 sb=0 sd=0 mult=1 m=1
XM4 net1 VC GND GND sky130_fd_pr__nfet_01v8 L=4 W=0.42 nf=1 ad='int((1 + 1)/2) * 0.42 / 1 * 0.29' as='int((1 + 2)/2) * 0.42 / 1 * 0.29'
+ pd='2*int((1 + 1)/2) * (0.42 / 1 + 0.29)' ps='2*int((1 + 2)/2) * (0.42 / 1 + 0.29)' nrd='0.29 / 0.42 '
+ nrs='0.29 / 0.42 ' sa=0 sb=0 sd=0 mult=1 m=1
XM1 net2 VC2 VDD VDD sky130_fd_pr__pfet_01v8_lvt L=4 W=0.42 nf=1 ad='int((1 + 1)/2) * 0.42 / 1 * 0.29'
+ as='int((1 + 2)/2) * 0.42 / 1 * 0.29' pd='2*int((1 + 1)/2) * (0.42 / 1 + 0.29)' ps='2*int((1 + 2)/2) * (0.42 / 1 + 0.29)'
+ nrd='0.29 / 0.42 ' nrs='0.29 / 0.42 ' sa=0 sb=0 sd=0 mult=1 m=1
XM2 VOUT VIN net2 VDD sky130_fd_pr__pfet_01v8_lvt L=0.35 W=1 nf=1 ad='int((1 + 1)/2) * 1 / 1 * 0.29'
+ as='int((1 + 2)/2) * 1 / 1 * 0.29' pd='2*int((1 + 1)/2) * (1 / 1 + 0.29)' ps='2*int((1 + 2)/2) * (1 / 1 + 0.29)'
+ nrd='0.29 / 1 ' nrs='0.29 / 1 ' sa=0 sb=0 sd=0 mult=1 m=1
.ends


* expanding   symbol:  LELO_SVOD_SKY130A/1812PS-564_imp.sym # of pins=2
** sym_path: design/LELO_SVOD_SKY130A/1812PS-564_imp.sym

.subckt 1812PS-564_imp port1 port2
X1 port1 port2 Model1D R1=70 R2=6.1 C= 7.71p K1=0.000001 K2=115.8 K3= 560u K4=0.000001 K5=0.000001
+ L=0 Is=0 a=0 L_Z0=0 L_EL=0 L_F0=0E6 PkZ=153558.837
.ends 1812PS-564_imp

* expanding   symbol:  LELO_SVOD_SKY130A/XGL6030-472_sat.sym # of pins=2
** sym_path: design/LELO_SVOD_SKY130A/XGL6030-472_sat.sym

.subckt XGL6030-472_sat port1 port2
X1 port1 port2 Model1C R1=5 R2=0.021 C=13.9p K1=0.000001 K2=1.05 K3= 4.7u K4=0.000001 K5=0.000001
+ L=4.5383E-06 Is=18.1418 a=0.725 L_Z0=0 L_EL=0 L_F0=0E6 PkZ=4358.77183
.ends XGL6030-472_sat

.end
